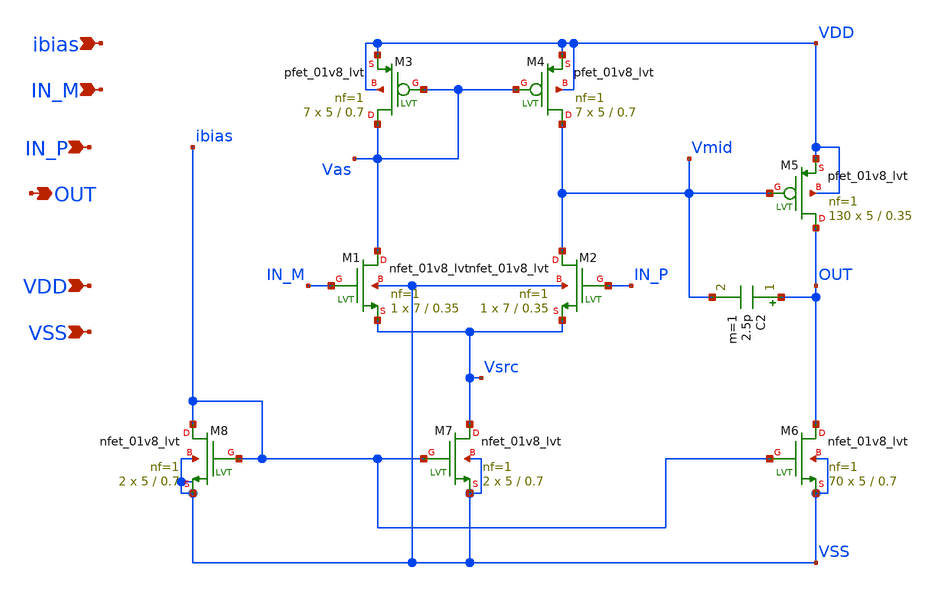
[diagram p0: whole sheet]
** sch_path: OTA_LASCAS2024.sch
**.subckt OTA_LASCAS2024 IN_M IN_P VDD VSS ibias OUT
*.ipin IN_M
*.ipin IN_P
*.ipin VDD
*.ipin VSS
*.ipin ibias
*.opin OUT
XM1 Vas IN_M Vsrc VSS sky130_fd_pr__nfet_01v8_lvt L=0.35 W=7 nf=1 ad='int((nf+1)/2) * W/nf * 0.29' as='int((nf+2)/2) * W/nf * 0.29'
+ pd='2*int((nf+1)/2) * (W/nf + 0.29)' ps='2*int((nf+2)/2) * (W/nf + 0.29)' nrd='0.29 / W' nrs='0.29 / W'
+ sa=0 sb=0 sd=0 mult=1 m=1
XM2 Vmid IN_P Vsrc VSS sky130_fd_pr__nfet_01v8_lvt L=0.35 W=7 nf=1 ad='int((nf+1)/2) * W/nf * 0.29' as='int((nf+2)/2) * W/nf * 0.29'
+ pd='2*int((nf+1)/2) * (W/nf + 0.29)' ps='2*int((nf+2)/2) * (W/nf + 0.29)' nrd='0.29 / W' nrs='0.29 / W'
+ sa=0 sb=0 sd=0 mult=1 m=1
XM3 Vas Vas VDD VDD sky130_fd_pr__pfet_01v8_lvt L=0.7 W=5 nf=1 ad='int((nf+1)/2) * W/nf * 0.29' as='int((nf+2)/2) * W/nf * 0.29'
+ pd='2*int((nf+1)/2) * (W/nf + 0.29)' ps='2*int((nf+2)/2) * (W/nf + 0.29)' nrd='0.29 / W' nrs='0.29 / W'
+ sa=0 sb=0 sd=0 mult=7 m=7
XM4 Vmid Vas VDD VDD sky130_fd_pr__pfet_01v8_lvt L=0.7 W=5 nf=1 ad='int((nf+1)/2) * W/nf * 0.29' as='int((nf+2)/2) * W/nf * 0.29'
+ pd='2*int((nf+1)/2) * (W/nf + 0.29)' ps='2*int((nf+2)/2) * (W/nf + 0.29)' nrd='0.29 / W' nrs='0.29 / W'
+ sa=0 sb=0 sd=0 mult=7 m=7
XM5 OUT Vmid VDD VDD sky130_fd_pr__pfet_01v8_lvt L=0.35 W=5 nf=1 ad='int((nf+1)/2) * W/nf * 0.29' as='int((nf+2)/2) * W/nf * 0.29'
+ pd='2*int((nf+1)/2) * (W/nf + 0.29)' ps='2*int((nf+2)/2) * (W/nf + 0.29)' nrd='0.29 / W' nrs='0.29 / W'
+ sa=0 sb=0 sd=0 mult=130 m=130
XM6 OUT ibias VSS VSS sky130_fd_pr__nfet_01v8_lvt L=0.7 W=5 nf=1 ad='int((nf+1)/2) * W/nf * 0.29' as='int((nf+2)/2) * W/nf * 0.29'
+ pd='2*int((nf+1)/2) * (W/nf + 0.29)' ps='2*int((nf+2)/2) * (W/nf + 0.29)' nrd='0.29 / W' nrs='0.29 / W'
+ sa=0 sb=0 sd=0 mult=70 m=70
XM7 Vsrc ibias VSS VSS sky130_fd_pr__nfet_01v8_lvt L=0.7 W=5 nf=1 ad='int((nf+1)/2) * W/nf * 0.29' as='int((nf+2)/2) * W/nf * 0.29'
+ pd='2*int((nf+1)/2) * (W/nf + 0.29)' ps='2*int((nf+2)/2) * (W/nf + 0.29)' nrd='0.29 / W' nrs='0.29 / W'
+ sa=0 sb=0 sd=0 mult=2 m=2
XM8 ibias ibias VSS VSS sky130_fd_pr__nfet_01v8_lvt L=0.7 W=5 nf=1 ad='int((nf+1)/2) * W/nf * 0.29' as='int((nf+2)/2) * W/nf * 0.29'
+ pd='2*int((nf+1)/2) * (W/nf + 0.29)' ps='2*int((nf+2)/2) * (W/nf + 0.29)' nrd='0.29 / W' nrs='0.29 / W'
+ sa=0 sb=0 sd=0 mult=2 m=2
C2 OUT Vmid 2.5p m=1
**.ends
.end
